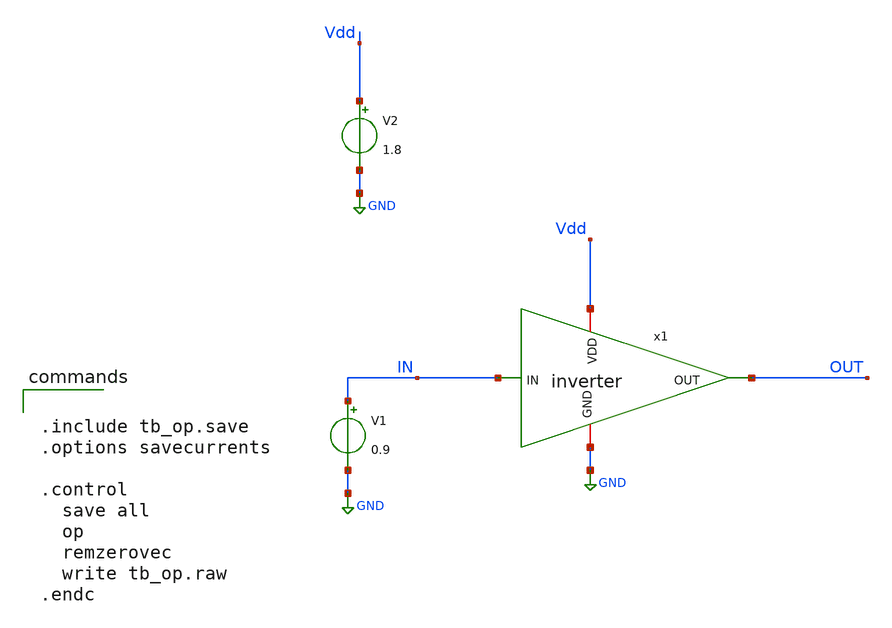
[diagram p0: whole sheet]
** sch_path: 01_xschem_ngspice/soluzioni/lab01/xschem/tb_op.sch
**.subckt tb_op
x1 Vdd IN OUT GND inverter
V1 IN GND 0.9
V2 Vdd GND 1.8
**** begin user architecture code

** opencircuitdesign pdks install
.lib $::SKYWATER_MODELS/sky130.lib.spice tt



.include tb_op.save
.options savecurrents

.control
  save all
  op
  remzerovec
  write tb_op.raw
.endc


**** end user architecture code
**.ends

* expanding   symbol:  inverter.sym # of pins=4
** sym_path: 01_xschem_ngspice/soluzioni/lab01/xschem/inverter.sym
** sch_path: 01_xschem_ngspice/soluzioni/lab01/xschem/inverter.sch
.subckt inverter VDD IN OUT GND
*.ipin IN
*.opin OUT
*.iopin VDD
*.iopin GND
XM1 OUT IN GND GND sky130_fd_pr__nfet_01v8 L=0.15 W=1 nf=1 ad='int((1 + 1)/2) * 1 / 1 * 0.29' as='int((1 + 2)/2) * 1 / 1 * 0.29'
+ pd='2*int((1 + 1)/2) * (1 / 1 + 0.29)' ps='2*int((1 + 2)/2) * (1 / 1 + 0.29)' nrd='0.29 / 1 ' nrs='0.29 / 1 '
+ sa=0 sb=0 sd=0 mult=1 m=1
XM2 OUT IN VDD VDD sky130_fd_pr__pfet_01v8 L=0.15 W=2 nf=1 ad='int((1 + 1)/2) * 2 / 1 * 0.29' as='int((1 + 2)/2) * 2 / 1 * 0.29'
+ pd='2*int((1 + 1)/2) * (2 / 1 + 0.29)' ps='2*int((1 + 2)/2) * (2 / 1 + 0.29)' nrd='0.29 / 2 ' nrs='0.29 / 2 '
+ sa=0 sb=0 sd=0 mult=1 m=1
.ends

.GLOBAL GND
.end
